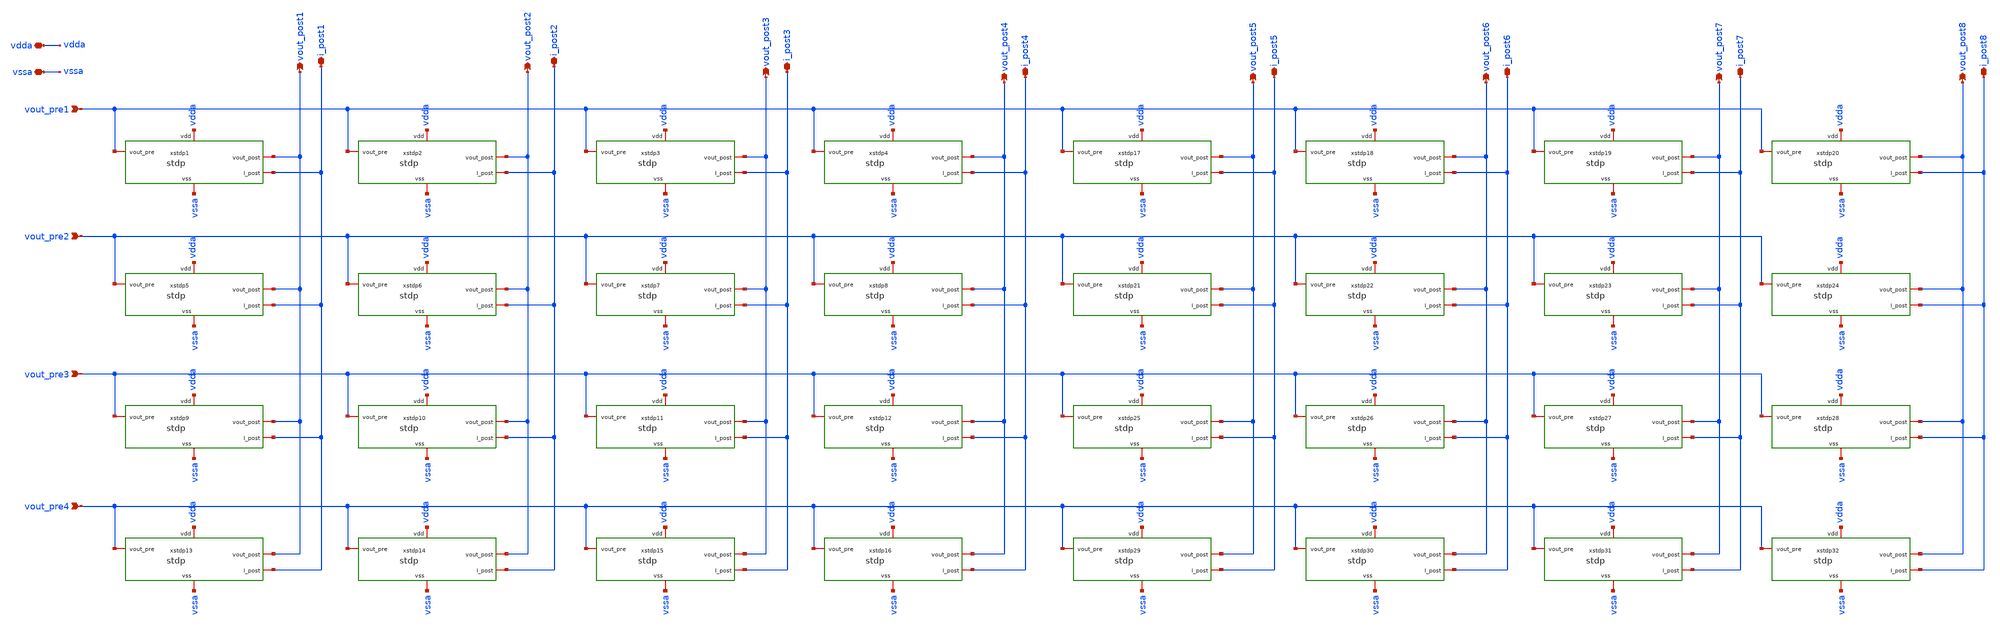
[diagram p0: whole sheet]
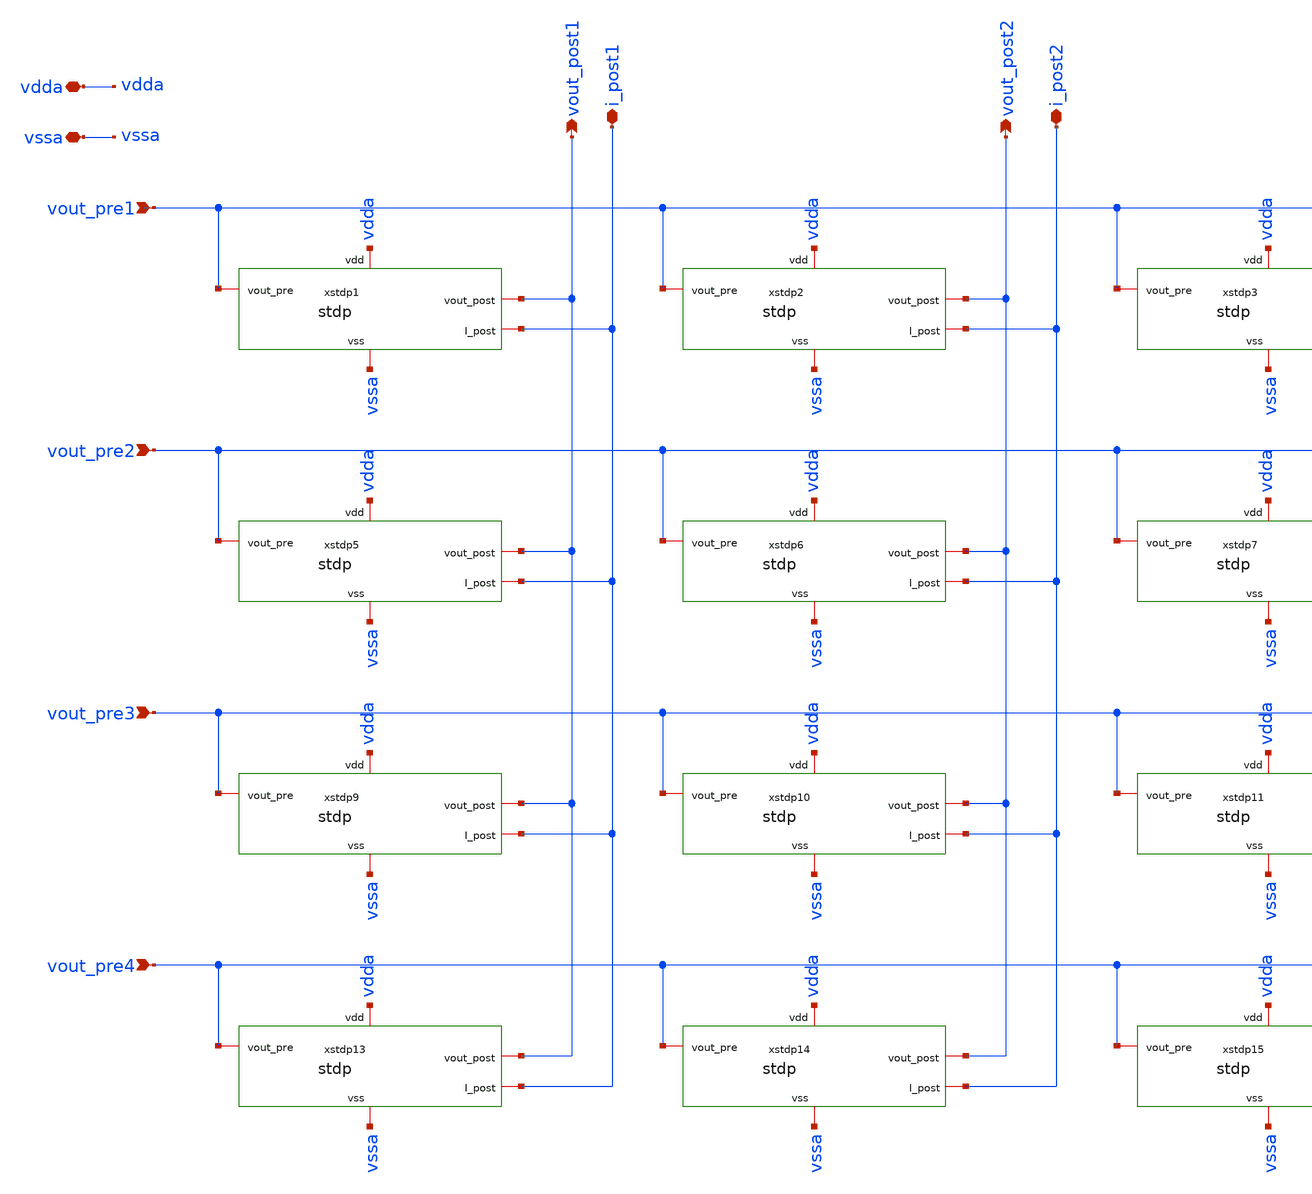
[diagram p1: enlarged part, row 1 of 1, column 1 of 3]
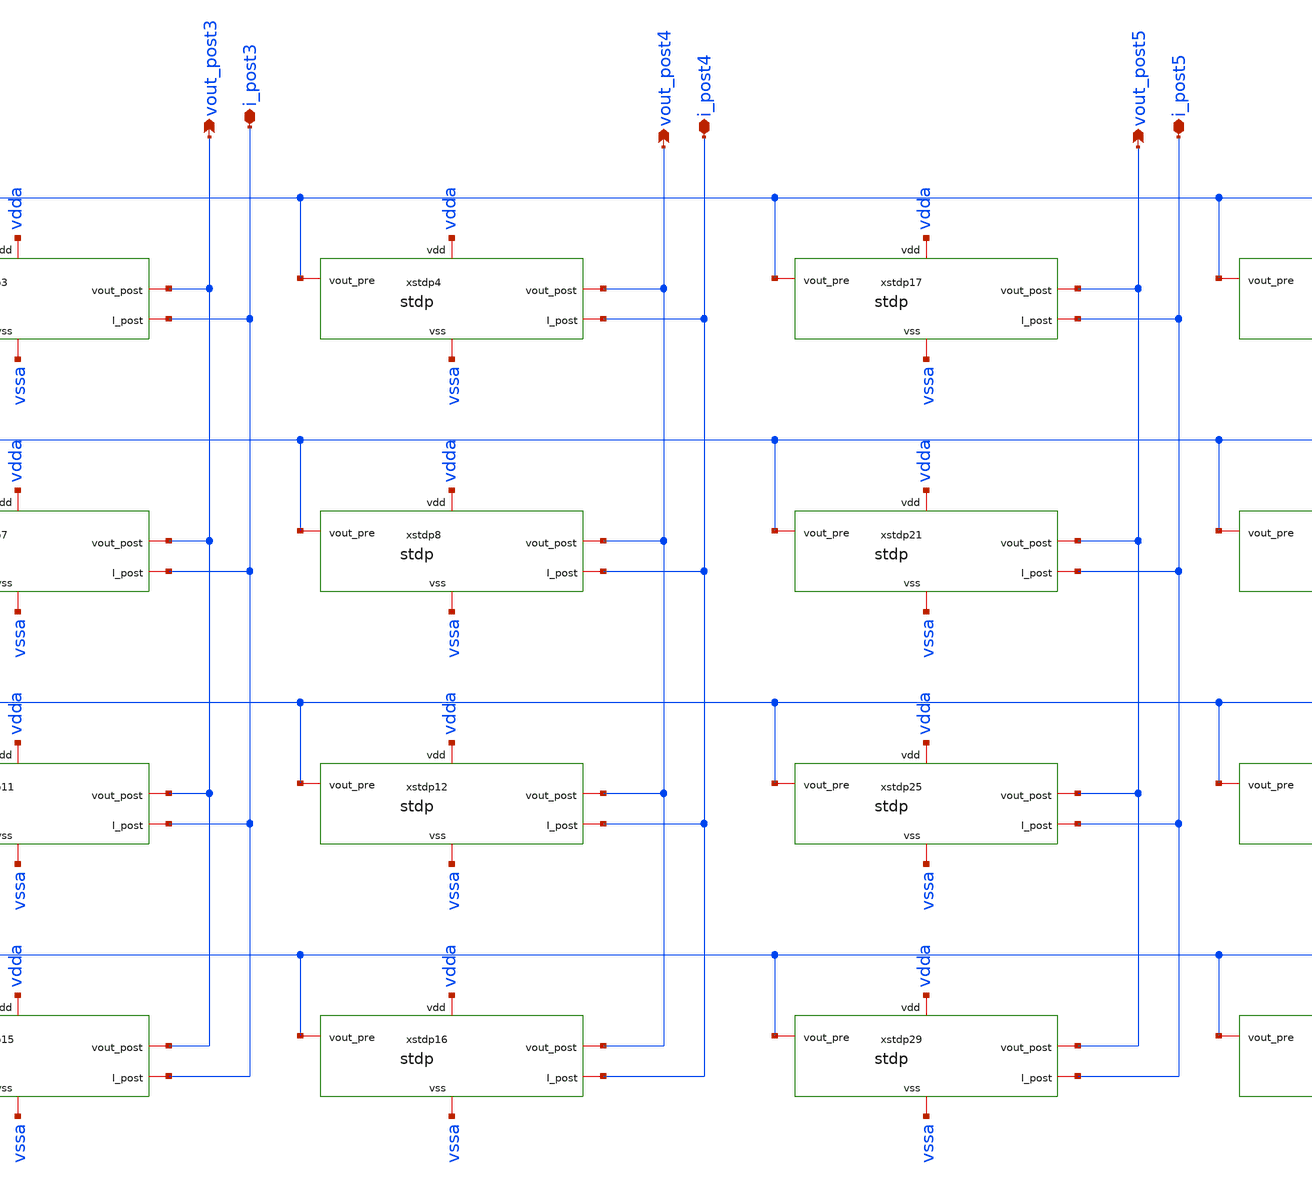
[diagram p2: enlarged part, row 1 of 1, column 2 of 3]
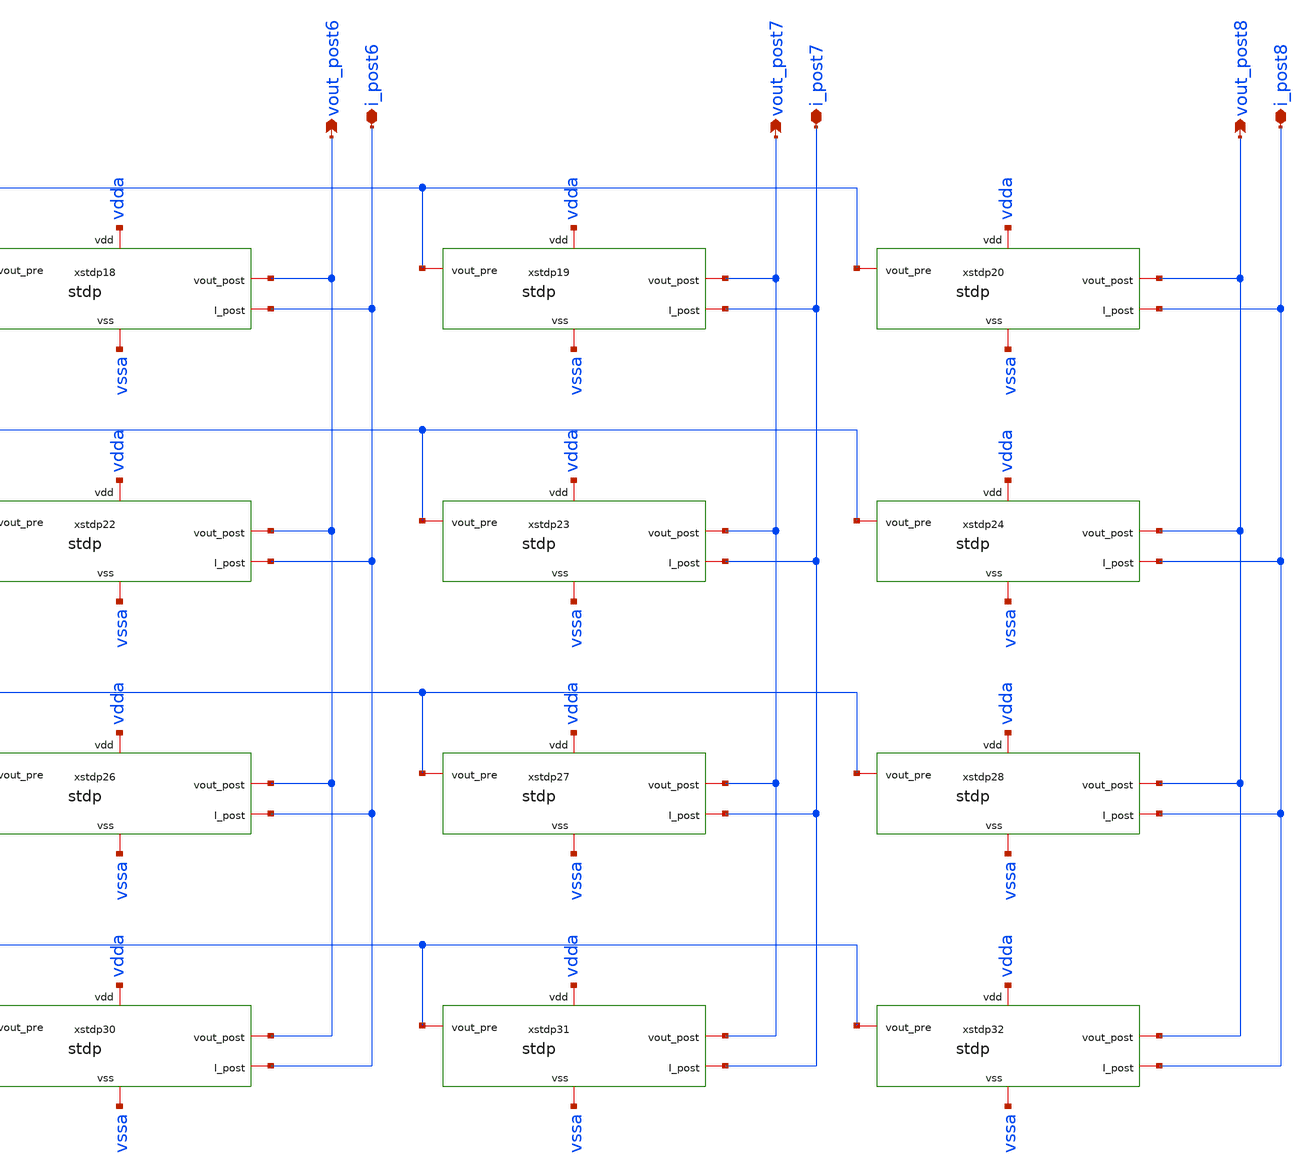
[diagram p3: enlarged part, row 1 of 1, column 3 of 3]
** sch_path: Synapse/stdp_4x8.sch
**.subckt stdp_4x8 vout_pre1 vout_post1 vdda vssa i_post1 i_post3 i_post4 vout_pre2 vout_pre3
*+ vout_pre4 vout_post2 vout_post3 vout_post4 i_post2 i_post5 vout_post5 i_post6 vout_post6 i_post7 vout_post7
*+ i_post8 vout_post8
*.ipin vout_pre1
*.opin vout_post1
*.iopin vdda
*.iopin vssa
*.iopin i_post1
*.iopin i_post3
*.iopin i_post4
*.ipin vout_pre2
*.ipin vout_pre3
*.ipin vout_pre4
*.opin vout_post2
*.opin vout_post3
*.opin vout_post4
*.iopin i_post2
*.iopin i_post5
*.opin vout_post5
*.iopin i_post6
*.opin vout_post6
*.iopin i_post7
*.opin vout_post7
*.iopin i_post8
*.opin vout_post8
xstdp1 vdda vssa vout_pre1 vout_post1 i_post1 stdp
xstdp2 vdda vssa vout_pre1 vout_post2 i_post2 stdp
xstdp3 vdda vssa vout_pre1 vout_post3 i_post3 stdp
xstdp4 vdda vssa vout_pre1 vout_post4 i_post4 stdp
xstdp5 vdda vssa vout_pre2 vout_post1 i_post1 stdp
xstdp6 vdda vssa vout_pre2 vout_post2 i_post2 stdp
xstdp7 vdda vssa vout_pre2 vout_post3 i_post3 stdp
xstdp8 vdda vssa vout_pre2 vout_post4 i_post4 stdp
xstdp9 vdda vssa vout_pre3 vout_post1 i_post1 stdp
xstdp10 vdda vssa vout_pre3 vout_post2 i_post2 stdp
xstdp11 vdda vssa vout_pre3 vout_post3 i_post3 stdp
xstdp12 vdda vssa vout_pre3 vout_post4 i_post4 stdp
xstdp13 vdda vssa vout_pre4 vout_post1 i_post1 stdp
xstdp14 vdda vssa vout_pre4 vout_post2 i_post2 stdp
xstdp15 vdda vssa vout_pre4 vout_post3 i_post3 stdp
xstdp16 vdda vssa vout_pre4 vout_post4 i_post4 stdp
xstdp17 vdda vssa vout_pre1 vout_post5 i_post5 stdp
xstdp18 vdda vssa vout_pre1 vout_post6 i_post6 stdp
xstdp19 vdda vssa vout_pre1 vout_post7 i_post7 stdp
xstdp20 vdda vssa vout_pre1 vout_post8 i_post8 stdp
xstdp21 vdda vssa vout_pre2 vout_post5 i_post5 stdp
xstdp22 vdda vssa vout_pre2 vout_post6 i_post6 stdp
xstdp23 vdda vssa vout_pre2 vout_post7 i_post7 stdp
xstdp24 vdda vssa vout_pre2 vout_post8 i_post8 stdp
xstdp25 vdda vssa vout_pre3 vout_post5 i_post5 stdp
xstdp26 vdda vssa vout_pre3 vout_post6 i_post6 stdp
xstdp27 vdda vssa vout_pre3 vout_post7 i_post7 stdp
xstdp28 vdda vssa vout_pre3 vout_post8 i_post8 stdp
xstdp29 vdda vssa vout_pre4 vout_post5 i_post5 stdp
xstdp30 vdda vssa vout_pre4 vout_post6 i_post6 stdp
xstdp31 vdda vssa vout_pre4 vout_post7 i_post7 stdp
xstdp32 vdda vssa vout_pre4 vout_post8 i_post8 stdp
**.ends

* expanding   symbol:  Synapse/stdp.sym # of pins=5
** sym_path: Synapse/stdp.sym
** sch_path: Synapse/stdp.sch
.subckt stdp vdd vss vout_pre vout_post I_post
*.iopin vdd
*.iopin vss
*.iopin vout_post
*.iopin vout_pre
*.iopin I_post
XM2 A vout_pre be vss sky130_fd_pr__nfet_01v8 L=0.15 W=7.5 nf=1 ad='int((nf+1)/2) * W/nf * 0.29' as='int((nf+2)/2) * W/nf * 0.29'
+ pd='2*int((nf+1)/2) * (W/nf + 0.29)' ps='2*int((nf+2)/2) * (W/nf + 0.29)' nrd='0.29 / W' nrs='0.29 / W'
+ sa=0 sb=0 sd=0 mult=1 m=1
XM3 be vout_post vss vss sky130_fd_pr__nfet_01v8 L=0.15 W=7.5 nf=1 ad='int((nf+1)/2) * W/nf * 0.29' as='int((nf+2)/2) * W/nf * 0.29'
+ pd='2*int((nf+1)/2) * (W/nf + 0.29)' ps='2*int((nf+2)/2) * (W/nf + 0.29)' nrd='0.29 / W' nrs='0.29 / W'
+ sa=0 sb=0 sd=0 mult=1 m=1
XM1 A vout_post te vss sky130_fd_pr__nfet_01v8 L=0.15 W=7.5 nf=1 ad='int((nf+1)/2) * W/nf * 0.29' as='int((nf+2)/2) * W/nf * 0.29'
+ pd='2*int((nf+1)/2) * (W/nf + 0.29)' ps='2*int((nf+2)/2) * (W/nf + 0.29)' nrd='0.29 / W' nrs='0.29 / W'
+ sa=0 sb=0 sd=0 mult=1 m=1
XM4 te vout_pre vss vss sky130_fd_pr__nfet_01v8 L=0.15 W=7.5 nf=1 ad='int((nf+1)/2) * W/nf * 0.29' as='int((nf+2)/2) * W/nf * 0.29'
+ pd='2*int((nf+1)/2) * (W/nf + 0.29)' ps='2*int((nf+2)/2) * (W/nf + 0.29)' nrd='0.29 / W' nrs='0.29 / W'
+ sa=0 sb=0 sd=0 mult=1 m=1
XR2 te be rram_v0
XM14 I_post A vdd vdd sky130_fd_pr__pfet_01v8 L=2.5 W=0.5 nf=1 ad='int((nf+1)/2) * W/nf * 0.29' as='int((nf+2)/2) * W/nf * 0.29'
+ pd='2*int((nf+1)/2) * (W/nf + 0.29)' ps='2*int((nf+2)/2) * (W/nf + 0.29)' nrd='0.29 / W' nrs='0.29 / W'
+ sa=0 sb=0 sd=0 mult=1 m=1
XM15 A A vdd vdd sky130_fd_pr__pfet_01v8 L=0.15 W=2.5 nf=1 ad='int((nf+1)/2) * W/nf * 0.29' as='int((nf+2)/2) * W/nf * 0.29'
+ pd='2*int((nf+1)/2) * (W/nf + 0.29)' ps='2*int((nf+2)/2) * (W/nf + 0.29)' nrd='0.29 / W' nrs='0.29 / W'
+ sa=0 sb=0 sd=0 mult=1 m=1
.ends

.end
